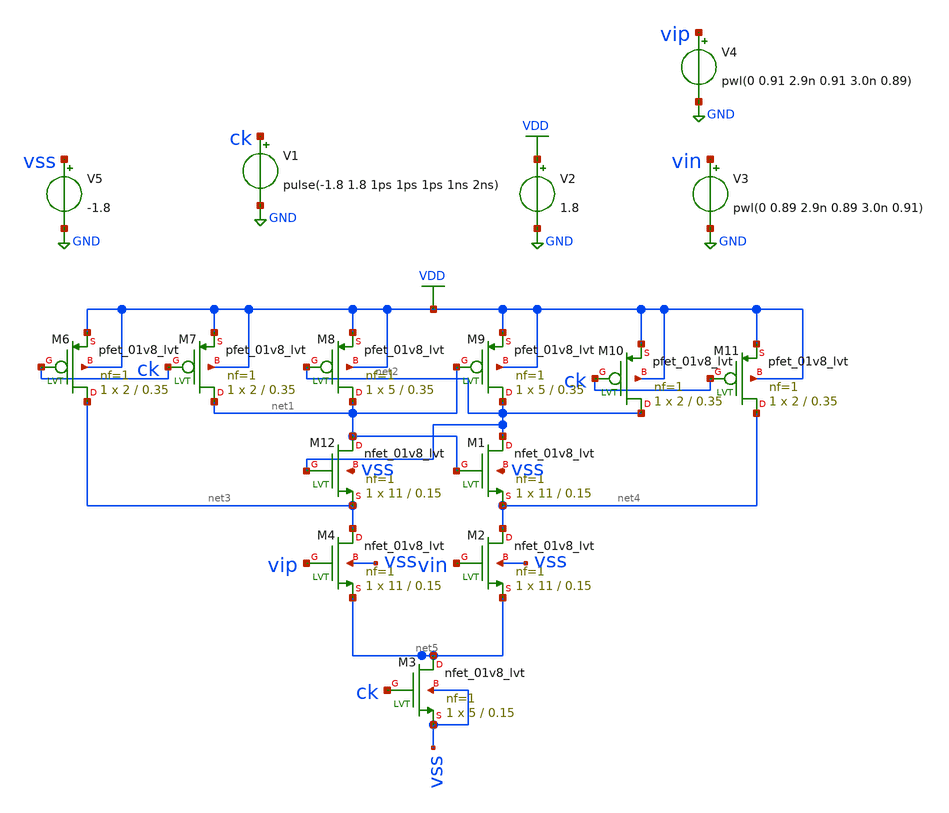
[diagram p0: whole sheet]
** sch_path: comparator_modified.sch
**.subckt comparator_modified
V1 ck GND pulse(-1.8 1.8 1ps 1ps 1ps 1ns 2ns)
V2 VDD GND 1.8
V3 vin GND pwl(0 0.89 2.9n 0.89 3.0n 0.91)
V4 vip GND pwl(0 0.91 2.9n 0.91 3.0n 0.89)
XM12 net1 net2 net3 vss sky130_fd_pr__nfet_01v8_lvt L=0.15 W=11 nf=1 ad='int((nf+1)/2) * W/nf * 0.29'
+ as='int((nf+2)/2) * W/nf * 0.29' pd='2*int((nf+1)/2) * (W/nf + 0.29)' ps='2*int((nf+2)/2) * (W/nf + 0.29)'
+ nrd='0.29 / W' nrs='0.29 / W' sa=0 sb=0 sd=0 mult=1 m=1
XM1 net2 net1 net4 vss sky130_fd_pr__nfet_01v8_lvt L=0.15 W=11 nf=1 ad='int((nf+1)/2) * W/nf * 0.29'
+ as='int((nf+2)/2) * W/nf * 0.29' pd='2*int((nf+1)/2) * (W/nf + 0.29)' ps='2*int((nf+2)/2) * (W/nf + 0.29)'
+ nrd='0.29 / W' nrs='0.29 / W' sa=0 sb=0 sd=0 mult=1 m=1
XM2 net4 vin net5 vss sky130_fd_pr__nfet_01v8_lvt L=0.15 W=11 nf=1 ad='int((nf+1)/2) * W/nf * 0.29' as='int((nf+2)/2) * W/nf * 0.29'
+ pd='2*int((nf+1)/2) * (W/nf + 0.29)' ps='2*int((nf+2)/2) * (W/nf + 0.29)' nrd='0.29 / W' nrs='0.29 / W'
+ sa=0 sb=0 sd=0 mult=1 m=1
XM4 net3 vip net5 vss sky130_fd_pr__nfet_01v8_lvt L=0.15 W=11 nf=1 ad='int((nf+1)/2) * W/nf * 0.29' as='int((nf+2)/2) * W/nf * 0.29'
+ pd='2*int((nf+1)/2) * (W/nf + 0.29)' ps='2*int((nf+2)/2) * (W/nf + 0.29)' nrd='0.29 / W' nrs='0.29 / W'
+ sa=0 sb=0 sd=0 mult=1 m=1
XM3 net5 ck vss vss sky130_fd_pr__nfet_01v8_lvt L=0.15 W=5 nf=1 ad='int((nf+1)/2) * W/nf * 0.29' as='int((nf+2)/2) * W/nf * 0.29'
+ pd='2*int((nf+1)/2) * (W/nf + 0.29)' ps='2*int((nf+2)/2) * (W/nf + 0.29)' nrd='0.29 / W' nrs='0.29 / W'
+ sa=0 sb=0 sd=0 mult=1 m=1
XM6 net3 ck VDD VDD sky130_fd_pr__pfet_01v8_lvt L=0.35 W=2 nf=1 ad='int((nf+1)/2) * W/nf * 0.29' as='int((nf+2)/2) * W/nf * 0.29'
+ pd='2*int((nf+1)/2) * (W/nf + 0.29)' ps='2*int((nf+2)/2) * (W/nf + 0.29)' nrd='0.29 / W' nrs='0.29 / W'
+ sa=0 sb=0 sd=0 mult=1 m=1
XM7 net1 ck VDD VDD sky130_fd_pr__pfet_01v8_lvt L=0.35 W=2 nf=1 ad='int((nf+1)/2) * W/nf * 0.29' as='int((nf+2)/2) * W/nf * 0.29'
+ pd='2*int((nf+1)/2) * (W/nf + 0.29)' ps='2*int((nf+2)/2) * (W/nf + 0.29)' nrd='0.29 / W' nrs='0.29 / W'
+ sa=0 sb=0 sd=0 mult=1 m=1
XM8 net1 net2 VDD VDD sky130_fd_pr__pfet_01v8_lvt L=0.35 W=5 nf=1 ad='int((nf+1)/2) * W/nf * 0.29' as='int((nf+2)/2) * W/nf * 0.29'
+ pd='2*int((nf+1)/2) * (W/nf + 0.29)' ps='2*int((nf+2)/2) * (W/nf + 0.29)' nrd='0.29 / W' nrs='0.29 / W'
+ sa=0 sb=0 sd=0 mult=1 m=1
XM9 net2 net1 VDD VDD sky130_fd_pr__pfet_01v8_lvt L=0.35 W=5 nf=1 ad='int((nf+1)/2) * W/nf * 0.29' as='int((nf+2)/2) * W/nf * 0.29'
+ pd='2*int((nf+1)/2) * (W/nf + 0.29)' ps='2*int((nf+2)/2) * (W/nf + 0.29)' nrd='0.29 / W' nrs='0.29 / W'
+ sa=0 sb=0 sd=0 mult=1 m=1
XM10 net2 ck VDD VDD sky130_fd_pr__pfet_01v8_lvt L=0.35 W=2 nf=1 ad='int((nf+1)/2) * W/nf * 0.29' as='int((nf+2)/2) * W/nf * 0.29'
+ pd='2*int((nf+1)/2) * (W/nf + 0.29)' ps='2*int((nf+2)/2) * (W/nf + 0.29)' nrd='0.29 / W' nrs='0.29 / W'
+ sa=0 sb=0 sd=0 mult=1 m=1
XM11 net4 ck VDD VDD sky130_fd_pr__pfet_01v8_lvt L=0.35 W=2 nf=1 ad='int((nf+1)/2) * W/nf * 0.29' as='int((nf+2)/2) * W/nf * 0.29'
+ pd='2*int((nf+1)/2) * (W/nf + 0.29)' ps='2*int((nf+2)/2) * (W/nf + 0.29)' nrd='0.29 / W' nrs='0.29 / W'
+ sa=0 sb=0 sd=0 mult=1 m=1
V5 vss GND -1.8
**** begin user architecture code

*.lib ~/open_pdks/sky130/sky130A/libs.tech/ngspice/sky130.lib.spice tt
.param mc_mm_switch=0
.param mc_pr_switch=0

.include ~/open_pdks/sky130/sky130A/libs.tech/ngspice/corners/tt/nonfet.spice

*model
.include ~/open_pdks/sky130/sky130A/libs.tech/ngspice/all.spice

*mosfet
.include ~/open_pdks/sky130/sky130A/libs.ref/sky130_fd_pr/spice/sky130_fd_pr__pfet_01v8__tt.corner.spice
.inclued ~/open_pdks/sky130/sky130A/libs.ref/sky130_fd_pr/spice/sky130_fd_pr__nfet_01v8__tt.corner.spice

*mismatch parameters
.include ~/open_pdks/sky130/sky130A/libs.ref/sky130_fd_pr/spice/sky130_fd_pr__pfet_01v8__mismatch.corner.spice
.include ~/open_pdks/sky130/sky130A/libs.ref/sky130_fd_pr/spice/sky130_fd_pr__nfet_01v8__mismatch.corner.spice

*mosfet
.include ~/open_pdks/sky130/sky130A/libs.ref/sky130_fd_pr/spice/sky130_fd_pr__pfet_01v8_lvt__tt.corner.spice
.inclued ~/open_pdks/sky130/sky130A/libs.ref/sky130_fd_pr/spice/sky130_fd_pr__nfet_01v8_lvt__tt.corner.spice

*mismatch parameters
.include ~/open_pdks/sky130/sky130A/libs.ref/sky130_fd_pr/spice/sky130_fd_pr__pfet_01v8_lvt__mismatch.corner.spice
.include ~/open_pdks/sky130/sky130A/libs.ref/sky130_fd_pr/spice/sky130_fd_pr__nfet_01v8_lvt__mismatch.corner.spice
.control
tran .005ns 8ns
plot v(net1) v(net2)
plot v(ck)
save all
.endc

**** end user architecture code
**.ends
.GLOBAL VDD
.GLOBAL GND
.end
